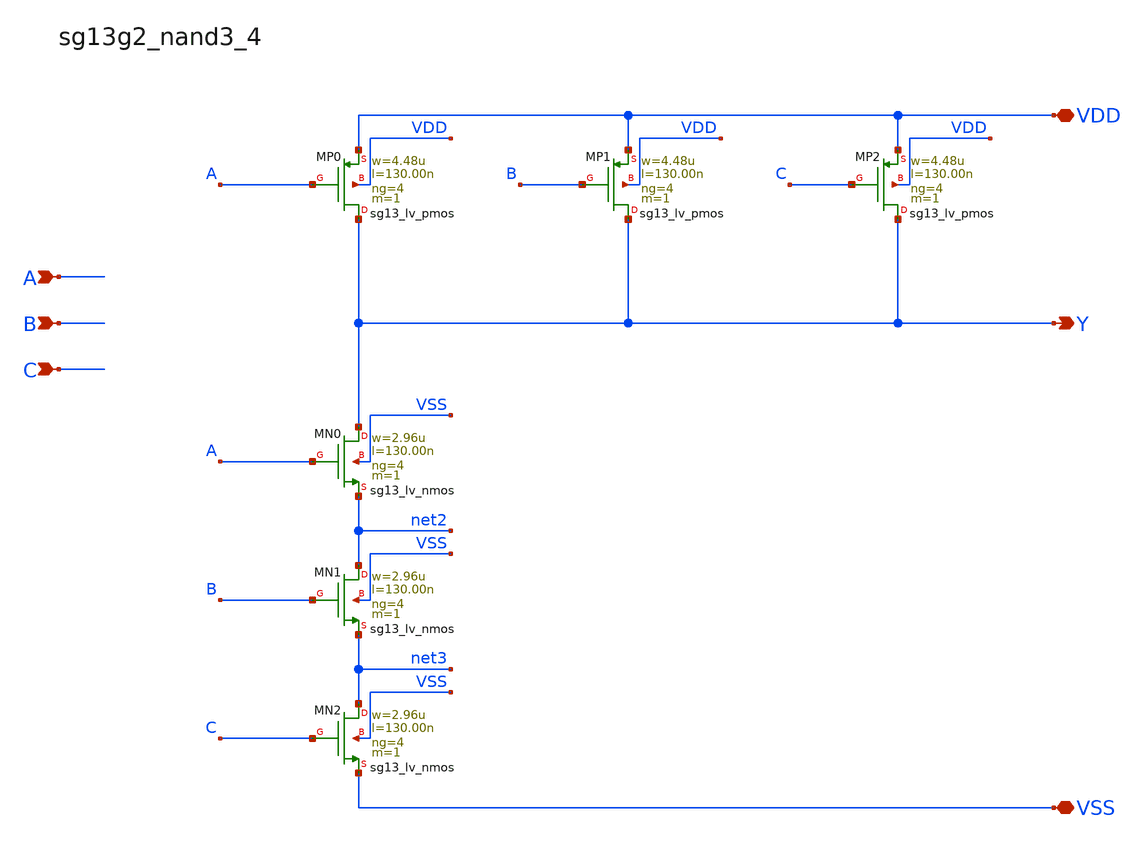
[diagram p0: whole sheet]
** sch_path: outputs/sg13g2_cells/cells/sg13g2_nand3_4/sg13g2_nand3_4.sch
**.subckt sg13g2_nand3_4 Y A B C VDD VSS
*.opin Y
*.ipin A
*.ipin B
*.ipin C
*.iopin VDD
*.iopin VSS
XMP0 Y A VDD VDD sg13_lv_pmos w=4.48u l=130.00n ng=4 m=1 mm_ok=1
XMP1 Y B VDD VDD sg13_lv_pmos w=4.48u l=130.00n ng=4 m=1 mm_ok=1
XMP2 Y C VDD VDD sg13_lv_pmos w=4.48u l=130.00n ng=4 m=1 mm_ok=1
XMN1 net2 B net3 VSS sg13_lv_nmos w=2.96u l=130.00n ng=4 m=1 mm_ok=1
XMN2 net3 C VSS VSS sg13_lv_nmos w=2.96u l=130.00n ng=4 m=1 mm_ok=1
XMN0 Y A net2 VSS sg13_lv_nmos w=2.96u l=130.00n ng=4 m=1 mm_ok=1
**.ends
.end
